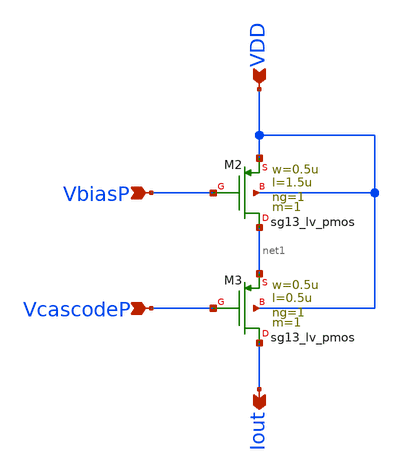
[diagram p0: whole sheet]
** sch_path: xschem/Pmirror_StdCell.sch
**.subckt Pmirror_StdCell VcascodeP VbiasP Iout VDD
*.ipin VcascodeP
*.ipin VbiasP
*.opin Iout
*.ipin VDD
XM2 net1 VbiasP VDD VDD sg13_lv_pmos w=0.5u l=1.5u ng=1 m=1 mm_ok=1
XM3 Iout VcascodeP net1 VDD sg13_lv_pmos w=0.5u l=0.5u ng=1 m=1 mm_ok=1
**.ends
.end
